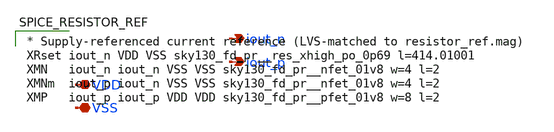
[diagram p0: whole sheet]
** sch_path: bvm_analog_tapeout/analog/bandgap/xschem/resistor_ref.sch
**.subckt resistor_ref iout_n iout_p VDD VSS
*.opin iout_n
*.opin iout_p
*.iopin VDD
*.iopin VSS
**** begin user architecture code

* Supply-referenced current reference (LVS-matched to resistor_ref.mag)
XRset iout_n VDD VSS sky130_fd_pr__res_xhigh_po_0p69 l=414.01001
XMN   iout_n iout_n VSS VSS sky130_fd_pr__nfet_01v8 w=4 l=2
XMNm  iout_p iout_n VSS VSS sky130_fd_pr__nfet_01v8 w=4 l=2
XMP   iout_p iout_p VDD VDD sky130_fd_pr__pfet_01v8 w=8 l=2

**** end user architecture code
**.ends
.end
